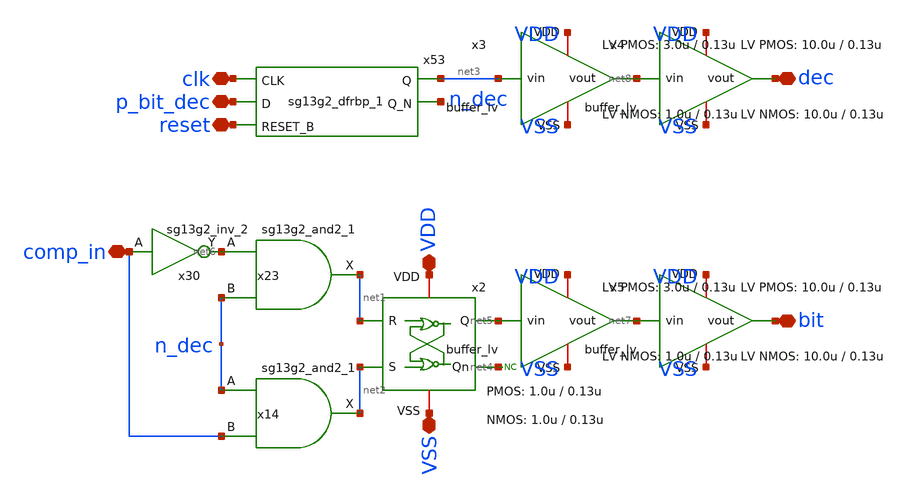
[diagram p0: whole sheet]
** sch_path: xschem/logic/bit_cell.sch
**.subckt bit_cell p_bit_dec clk reset comp_in VDD VSS bit dec
*.iopin p_bit_dec
*.iopin clk
*.iopin reset
*.iopin comp_in
*.iopin VDD
*.iopin VSS
*.iopin bit
*.iopin dec
x1 VDD net2 net4 VSS net5 net1 SR_latch W_P_SR=1.0u L_P_SR=0.13u W_N_SR=1.0u L_N_SR=0.13u
x23 net1 net6 n_dec VDD VSS sg13g2_and2_1
x14 net2 n_dec comp_in VDD VSS sg13g2_and2_1
x30 net6 comp_in VDD VSS sg13g2_inv_2
x53 net3 n_dec clk p_bit_dec reset VDD VSS sg13g2_dfrbp_1
* noconn #net4
x2 VDD net5 net7 VSS buffer_lv W_P_INV=3.0u L_P_INV=0.13u W_N_INV=1.0u L_N_INV=0.13u
x3 VDD net3 net8 VSS buffer_lv W_P_INV=3.0u L_P_INV=0.13u W_N_INV=1.0u L_N_INV=0.13u
x4 VDD net8 dec VSS buffer_lv W_P_INV=10.0u L_P_INV=0.13u W_N_INV=10.0u L_N_INV=0.13u
x5 VDD net7 bit VSS buffer_lv W_P_INV=10.0u L_P_INV=0.13u W_N_INV=10.0u L_N_INV=0.13u
**.ends
.end
